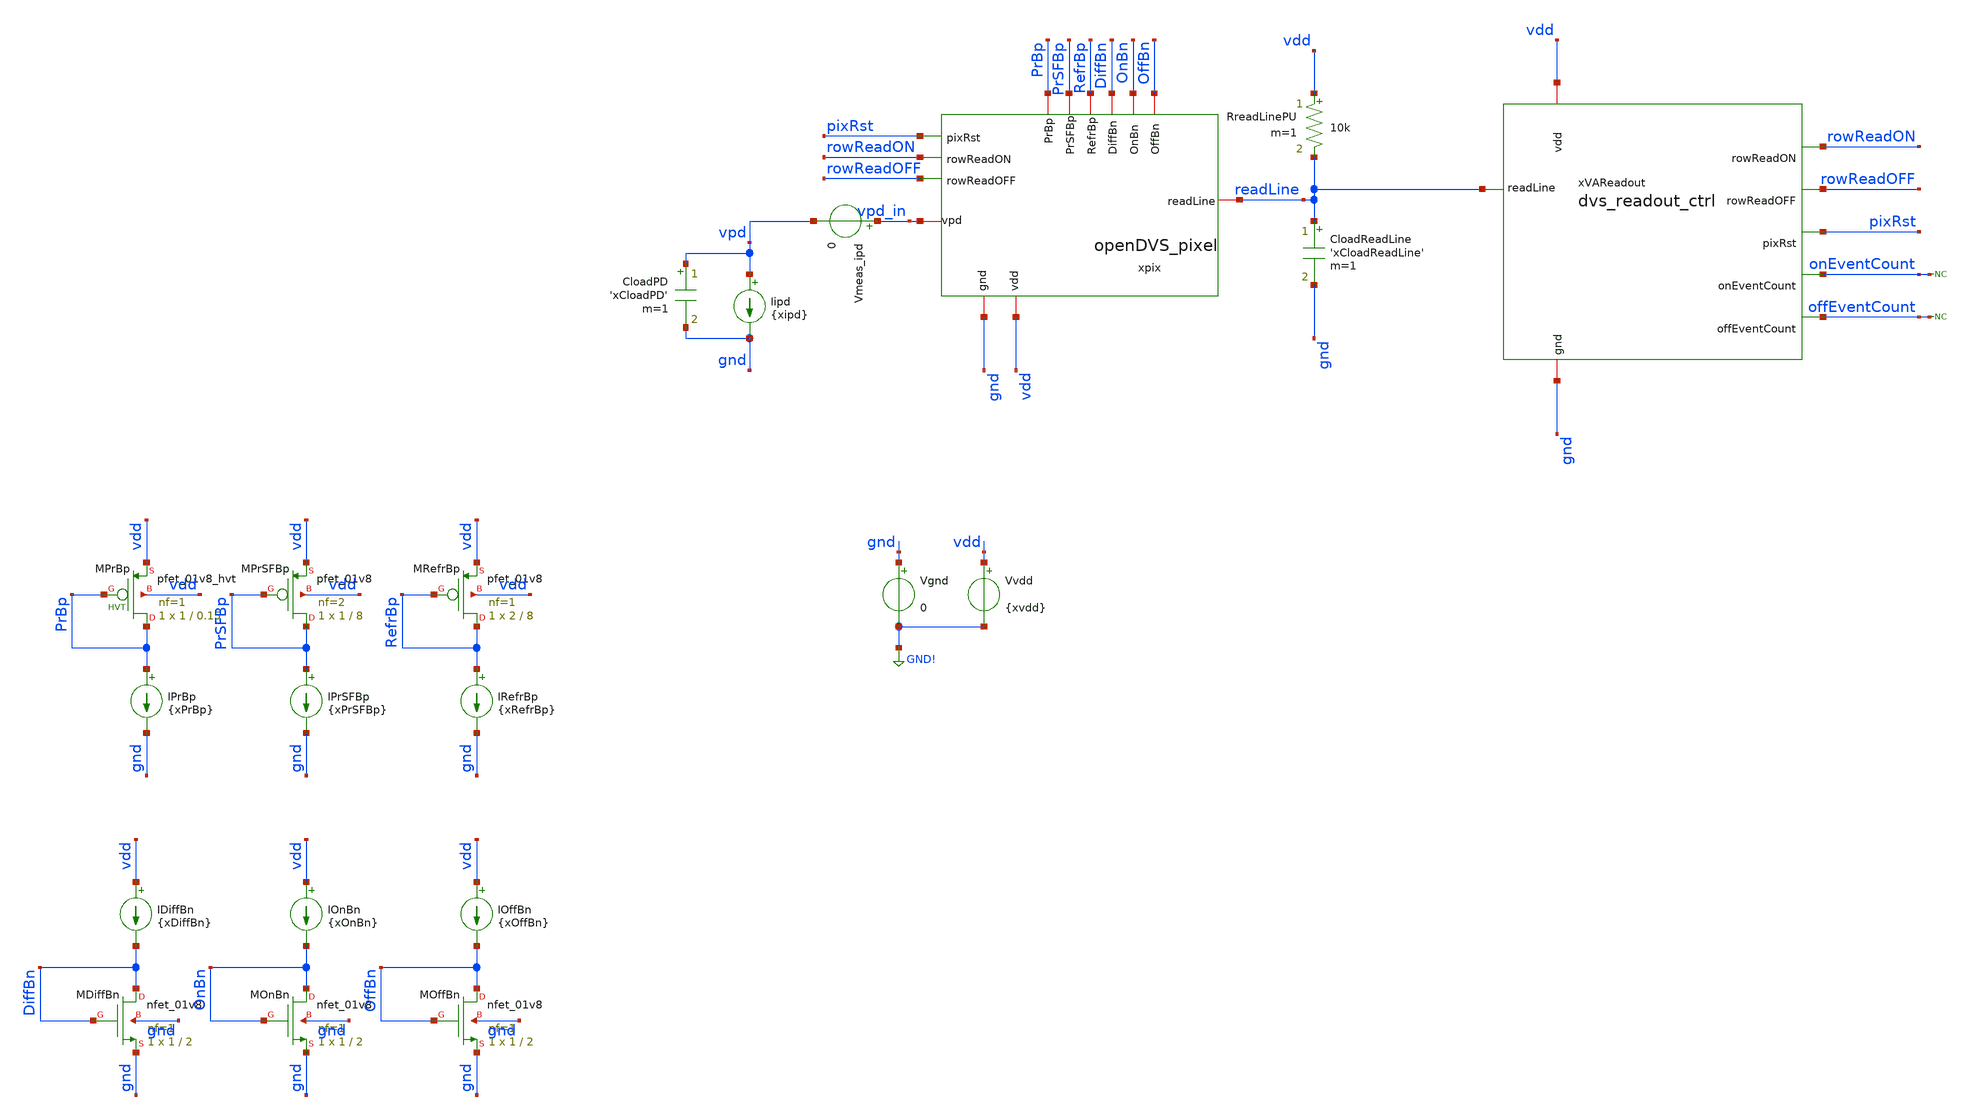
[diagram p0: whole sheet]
** sch_path: analog/klayout/production/final_merge_20260923/testbenches/cace/analog/xschem/pixel_tb.sch
**.subckt pixel_tb
xpix rowReadON vdd PrBp gnd vpd_in rowReadOFF pixRst PrSFBp DiffBn OnBn OffBn RefrBp readLine
+ openDVS_pixel
Vgnd gnd GND! 0
Vvdd vdd GND! {xvdd}
Iipd vpd gnd {xipd}
IRefrBp RefrBp gnd {xRefrBp}
XMRefrBp RefrBp RefrBp vdd vdd sky130_fd_pr__pfet_01v8 L=8 W=2 nf=1 ad='int((1 + 1)/2) * 2 / 1 * 0.29'
+ as='int((1 + 2)/2) * 2 / 1 * 0.29' pd='2*int((1 + 1)/2) * (2 / 1 + 0.29)' ps='2*int((1 + 2)/2) * (2 / 1 + 0.29)'
+ nrd='0.29 / 2 ' nrs='0.29 / 2 ' sa=0 sb=0 sd=0 mult=1 m=1
IPrBp PrBp gnd {xPrBp}
XMPrBp PrBp PrBp vdd vdd sky130_fd_pr__pfet_01v8_hvt L=0.15 W=1 nf=1 ad='int((1 + 1)/2) * 1 / 1 * 0.29'
+ as='int((1 + 2)/2) * 1 / 1 * 0.29' pd='2*int((1 + 1)/2) * (1 / 1 + 0.29)' ps='2*int((1 + 2)/2) * (1 / 1 + 0.29)'
+ nrd='0.29 / 1 ' nrs='0.29 / 1 ' sa=0 sb=0 sd=0 mult=1 m=1
IPrSFBp PrSFBp gnd {xPrSFBp}
XMDiffBn DiffBn DiffBn gnd gnd sky130_fd_pr__nfet_01v8 L=2 W=1 nf=1 ad='int((1 + 1)/2) * 1 / 1 * 0.29'
+ as='int((1 + 2)/2) * 1 / 1 * 0.29' pd='2*int((1 + 1)/2) * (1 / 1 + 0.29)' ps='2*int((1 + 2)/2) * (1 / 1 + 0.29)'
+ nrd='0.29 / 1 ' nrs='0.29 / 1 ' sa=0 sb=0 sd=0 mult=1 m=1
IDiffBn vdd DiffBn {xDiffBn}
XMOnBn OnBn OnBn gnd gnd sky130_fd_pr__nfet_01v8 L=2 W=1 nf=1 ad='int((1 + 1)/2) * 1 / 1 * 0.29' as='int((1 + 2)/2) * 1 / 1 * 0.29'
+ pd='2*int((1 + 1)/2) * (1 / 1 + 0.29)' ps='2*int((1 + 2)/2) * (1 / 1 + 0.29)' nrd='0.29 / 1 ' nrs='0.29 / 1 '
+ sa=0 sb=0 sd=0 mult=1 m=1
IOnBn vdd OnBn {xOnBn}
XMOffBn OffBn OffBn gnd gnd sky130_fd_pr__nfet_01v8 L=2 W=1 nf=1 ad='int((1 + 1)/2) * 1 / 1 * 0.29' as='int((1 + 2)/2) * 1 / 1 * 0.29'
+ pd='2*int((1 + 1)/2) * (1 / 1 + 0.29)' ps='2*int((1 + 2)/2) * (1 / 1 + 0.29)' nrd='0.29 / 1 ' nrs='0.29 / 1 '
+ sa=0 sb=0 sd=0 mult=1 m=1
IOffBn vdd OffBn {xOffBn}
CloadReadLine readLine gnd 'xCloadReadLine' m=1
CloadPD vpd gnd 'xCloadPD' m=1
Vmeas_ipd vpd_in vpd 0
XMPrSFBp PrSFBp PrSFBp vdd vdd sky130_fd_pr__pfet_01v8 L=8 W=1 nf=2 ad='int((2 + 1)/2) * 1 / 2 * 0.29'
+ as='int((2 + 2)/2) * 1 / 2 * 0.29' pd='2*int((2 + 1)/2) * (1 / 2 + 0.29)' ps='2*int((2 + 2)/2) * (1 / 2 + 0.29)'
+ nrd='0.29 / 1 ' nrs='0.29 / 1 ' sa=0 sb=0 sd=0 mult=1 m=1
RreadLinePU vdd readLine 10k m=1
xVAReadout readLine rowReadON rowReadOFF pixRst onEventCount offEventCount vdd gnd dvs_readout_ctrl
* noconn onEventCount
* noconn offEventCount
**** begin user architecture code

** opencircuitdesign pdks install
.lib $::SKYWATER_MODELS/sky130.lib.spice tt



.include /home/rpgraca/research/projects/telluride/2025/nic_eventcam/nic2025_openDVS/analog/xschem/dvs_readout_ctrl.spice

** Convergence options for nA-range weak-inversion pixel circuit
** gmin=1e-15: at 1V node this is 1fA shunt, negligible vs nA signals
** method=gear: damps numerical ringing on stiff circuits (fast digital + slow analog)
** trtol=1: conservative timestep control prevents overshoot at edges
.option gmin=1e-16 abstol=1e-15 vntol=1e-9 reltol=1e-4 chgtol=1e-16
.option method=gear maxord=2 trtol=1
.option itl1=500 itl2=200 itl4=50
.option gminsteps=200 srcsteps=200
.option ramptime=100n

.param xvdd = 1.8
.param xipd = 1e-9
.param xPrBp = 10n
.param xPrSFBp = 100p
.param xRefrBp = 4n
.param xDiffBn = 10n
.param xOnBn = 100n
.param xOffBn = 1n

.param xtr = 1n
.param xtperRead = 3u
.param xtdReadON = 100n
.param xtlenReadON = 950n
.param xtlenReadOFF = 950n
.param xtlenRstPhase = 950n
.param xtdReadOFF = 'xtdReadON+xtlenReadON+10n'
.param xtdRstPhase = 'xtdReadOFF+xtlenReadOFF+10n'
.param xtdRowSel = 50n
.param xtperRowSel = '2*xtperRead'

.param xCloadPD = 30f
.param xCloadReadLine = 300f
.param xCloadRowReadON = 300f
.param xCloadRowReadOFF = 300f
.param xCloadPixRst = 300f

*Small Iphoto testing
Iphoto1 vpd gnd pulse(50n 100n 120m 50m 50m 59.9m 300m)
Iphoto2 vpd gnd pulse(50n 25n 240m 50m 50m 59.9m 300m)

.control

	save all
	op
	tran 100n 390m
        write pixel_tb.raw
.endc


**** end user architecture code
**.ends

* expanding   symbol:  openDVS_pixel.sym # of pins=13
** sym_path: analog/xschem/openDVS_pixel.sym
** sch_path: analog/xschem/openDVS_pixel.sch
.subckt openDVS_pixel rowReadON vdd PrBp gnd vpd rowReadOFF pixRst PrSFBp DiffBn OnBn OffBn RefrBp
+ readLine
*.ipin rowReadON
*.iopin PrBp
*.iopin vdd
*.iopin vpd
*.iopin PrSFBp
*.iopin gnd
*.iopin DiffBn
*.iopin OnBn
*.iopin OffBn
*.ipin rowReadOFF
*.iopin readLine
*.ipin pixRst
*.iopin RefrBp
XC1 vsf vd sky130_fd_pr__cap_mim_m3_1 W=1 L=1 MF=16 m=16
XMpd vdd vpr vpd gnd sky130_fd_pr__nfet_01v8 L=0.15 W=0.5 nf=1 ad='int((1 + 1)/2) * 0.5 / 1 * 0.29' as='int((1 + 2)/2) * 0.5 / 1 * 0.29'
+ pd='2*int((1 + 1)/2) * (0.5 / 1 + 0.29)' ps='2*int((1 + 2)/2) * (0.5 / 1 + 0.29)' nrd='0.29 / 0.5 ' nrs='0.29 / 0.5 '
+ sa=0 sb=0 sd=0 mult=1 m=1
XMpr_amp vpr vpd gnd gnd sky130_fd_pr__nfet_01v8 L=0.15 W=0.5 nf=1 ad='int((1 + 1)/2) * 0.5 / 1 * 0.29'
+ as='int((1 + 2)/2) * 0.5 / 1 * 0.29' pd='2*int((1 + 1)/2) * (0.5 / 1 + 0.29)' ps='2*int((1 + 2)/2) * (0.5 / 1 + 0.29)'
+ nrd='0.29 / 0.5 ' nrs='0.29 / 0.5 ' sa=0 sb=0 sd=0 mult=1 m=1
XD1 gnd vpd sky130_fd_pr__photodiode area=25 perim=20
XC2 vd vdiff sky130_fd_pr__cap_mim_m3_1 W=1 L=1 MF=2 m=2
XMchAmpBias vdiff DiffBn gnd gnd sky130_fd_pr__nfet_01v8 L=2 W=1 nf=1 ad='int((1 + 1)/2) * 1 / 1 * 0.29'
+ as='int((1 + 2)/2) * 1 / 1 * 0.29' pd='2*int((1 + 1)/2) * (1 / 1 + 0.29)' ps='2*int((1 + 2)/2) * (1 / 1 + 0.29)'
+ nrd='0.29 / 1 ' nrs='0.29 / 1 ' sa=0 sb=0 sd=0 mult=1 m=1
XMonBias ON OnBn gnd gnd sky130_fd_pr__nfet_01v8 L=2 W=1 nf=1 ad='int((1 + 1)/2) * 1 / 1 * 0.29' as='int((1 + 2)/2) * 1 / 1 * 0.29'
+ pd='2*int((1 + 1)/2) * (1 / 1 + 0.29)' ps='2*int((1 + 2)/2) * (1 / 1 + 0.29)' nrd='0.29 / 1 ' nrs='0.29 / 1 '
+ sa=0 sb=0 sd=0 mult=1 m=1
XMoffBias nOFF OffBn gnd gnd sky130_fd_pr__nfet_01v8 L=2 W=1 nf=1 ad='int((1 + 1)/2) * 1 / 1 * 0.29'
+ as='int((1 + 2)/2) * 1 / 1 * 0.29' pd='2*int((1 + 1)/2) * (1 / 1 + 0.29)' ps='2*int((1 + 2)/2) * (1 / 1 + 0.29)'
+ nrd='0.29 / 1 ' nrs='0.29 / 1 ' sa=0 sb=0 sd=0 mult=1 m=1
XMswON readLine rowReadON readLineONpd gnd sky130_fd_pr__nfet_01v8 L=0.15 W=0.5 nf=1 ad='int((1 + 1)/2) * 0.5 / 1 * 0.29'
+ as='int((1 + 2)/2) * 0.5 / 1 * 0.29' pd='2*int((1 + 1)/2) * (0.5 / 1 + 0.29)' ps='2*int((1 + 2)/2) * (0.5 / 1 + 0.29)'
+ nrd='0.29 / 0.5 ' nrs='0.29 / 0.5 ' sa=0 sb=0 sd=0 mult=1 m=1
XMoutON readLineONpd ON gnd gnd sky130_fd_pr__nfet_01v8 L=0.15 W=0.5 nf=1 ad='int((1 + 1)/2) * 0.5 / 1 * 0.29'
+ as='int((1 + 2)/2) * 0.5 / 1 * 0.29' pd='2*int((1 + 1)/2) * (0.5 / 1 + 0.29)' ps='2*int((1 + 2)/2) * (0.5 / 1 + 0.29)'
+ nrd='0.29 / 0.5 ' nrs='0.29 / 0.5 ' sa=0 sb=0 sd=0 mult=1 m=1
XMswOFF readLine rowReadOFF readLineOFFpd gnd sky130_fd_pr__nfet_01v8 L=0.15 W=0.5 nf=1 ad='int((1 + 1)/2) * 0.5 / 1 * 0.29'
+ as='int((1 + 2)/2) * 0.5 / 1 * 0.29' pd='2*int((1 + 1)/2) * (0.5 / 1 + 0.29)' ps='2*int((1 + 2)/2) * (0.5 / 1 + 0.29)'
+ nrd='0.29 / 0.5 ' nrs='0.29 / 0.5 ' sa=0 sb=0 sd=0 mult=1 m=1
XMoutOFF readLineOFFpd nOFF gnd gnd sky130_fd_pr__nfet_01v8 L=0.15 W=0.5 nf=1 ad='int((1 + 1)/2) * 0.5 / 1 * 0.29'
+ as='int((1 + 2)/2) * 0.5 / 1 * 0.29' pd='2*int((1 + 1)/2) * (0.5 / 1 + 0.29)' ps='2*int((1 + 2)/2) * (0.5 / 1 + 0.29)'
+ nrd='0.29 / 0.5 ' nrs='0.29 / 0.5 ' sa=0 sb=0 sd=0 mult=1 m=1
XMrst vdiff nRst vd vdd sky130_fd_pr__pfet_01v8_hvt L=0.15 W=1 nf=1 ad='int((1 + 1)/2) * 1 / 1 * 0.29'
+ as='int((1 + 2)/2) * 1 / 1 * 0.29' pd='2*int((1 + 1)/2) * (1 / 1 + 0.29)' ps='2*int((1 + 2)/2) * (1 / 1 + 0.29)'
+ nrd='0.29 / 1 ' nrs='0.29 / 1 ' sa=0 sb=0 sd=0 mult=1 m=1
XMprBias vpr PrBp vdd vdd sky130_fd_pr__pfet_01v8_hvt L=0.15 W=1 nf=1 ad='int((1 + 1)/2) * 1 / 1 * 0.29'
+ as='int((1 + 2)/2) * 1 / 1 * 0.29' pd='2*int((1 + 1)/2) * (1 / 1 + 0.29)' ps='2*int((1 + 2)/2) * (1 / 1 + 0.29)'
+ nrd='0.29 / 1 ' nrs='0.29 / 1 ' sa=0 sb=0 sd=0 mult=1 m=1
XMsfBias vsf PrSFBp vdd vdd sky130_fd_pr__pfet_01v8_hvt L=8 W=2 nf=1 ad='int((1 + 1)/2) * 2 / 1 * 0.29'
+ as='int((1 + 2)/2) * 2 / 1 * 0.29' pd='2*int((1 + 1)/2) * (2 / 1 + 0.29)' ps='2*int((1 + 2)/2) * (2 / 1 + 0.29)'
+ nrd='0.29 / 2 ' nrs='0.29 / 2 ' sa=0 sb=0 sd=0 mult=1 m=1
XMchAmp vdiff vd vdd vdd sky130_fd_pr__pfet_01v8_hvt L=2 W=1 nf=1 ad='int((1 + 1)/2) * 1 / 1 * 0.29'
+ as='int((1 + 2)/2) * 1 / 1 * 0.29' pd='2*int((1 + 1)/2) * (1 / 1 + 0.29)' ps='2*int((1 + 2)/2) * (1 / 1 + 0.29)'
+ nrd='0.29 / 1 ' nrs='0.29 / 1 ' sa=0 sb=0 sd=0 mult=1 m=1
XMon ON vdiff vdd vdd sky130_fd_pr__pfet_01v8_hvt L=2 W=1 nf=1 ad='int((1 + 1)/2) * 1 / 1 * 0.29' as='int((1 + 2)/2) * 1 / 1 * 0.29'
+ pd='2*int((1 + 1)/2) * (1 / 1 + 0.29)' ps='2*int((1 + 2)/2) * (1 / 1 + 0.29)' nrd='0.29 / 1 ' nrs='0.29 / 1 '
+ sa=0 sb=0 sd=0 mult=1 m=1
XMoff nOFF vdiff vdd vdd sky130_fd_pr__pfet_01v8_hvt L=2 W=1 nf=1 ad='int((1 + 1)/2) * 1 / 1 * 0.29'
+ as='int((1 + 2)/2) * 1 / 1 * 0.29' pd='2*int((1 + 1)/2) * (1 / 1 + 0.29)' ps='2*int((1 + 2)/2) * (1 / 1 + 0.29)'
+ nrd='0.29 / 1 ' nrs='0.29 / 1 ' sa=0 sb=0 sd=0 mult=1 m=1
XMrefrInv nRst pixRst gnd gnd sky130_fd_pr__nfet_01v8 L=0.15 W=0.5 nf=1 ad='int((1 + 1)/2) * 0.5 / 1 * 0.29'
+ as='int((1 + 2)/2) * 0.5 / 1 * 0.29' pd='2*int((1 + 1)/2) * (0.5 / 1 + 0.29)' ps='2*int((1 + 2)/2) * (0.5 / 1 + 0.29)'
+ nrd='0.29 / 0.5 ' nrs='0.29 / 0.5 ' sa=0 sb=0 sd=0 mult=1 m=1
XMrefrBias nRst RefrBp vdd vdd sky130_fd_pr__pfet_01v8_hvt L=8 W=2 nf=1 ad='int((1 + 1)/2) * 2 / 1 * 0.29'
+ as='int((1 + 2)/2) * 2 / 1 * 0.29' pd='2*int((1 + 1)/2) * (2 / 1 + 0.29)' ps='2*int((1 + 2)/2) * (2 / 1 + 0.29)'
+ nrd='0.29 / 2 ' nrs='0.29 / 2 ' sa=0 sb=0 sd=0 mult=1 m=1
XMcapRefr vdd nRst net1 vdd sky130_fd_pr__pfet_01v8_hvt L=8 W=8 nf=1 ad='int((1 + 1)/2) * 8 / 1 * 0.29'
+ as='int((1 + 2)/2) * 8 / 1 * 0.29' pd='2*int((1 + 1)/2) * (8 / 1 + 0.29)' ps='2*int((1 + 2)/2) * (8 / 1 + 0.29)'
+ nrd='0.29 / 8 ' nrs='0.29 / 8 ' sa=0 sb=0 sd=0 mult=1 m=1
XMsfBias1 gnd vpr vsf vdd sky130_fd_pr__pfet_01v8_hvt L=2 W=1 nf=1 ad='int((1 + 1)/2) * 1 / 1 * 0.29'
+ as='int((1 + 2)/2) * 1 / 1 * 0.29' pd='2*int((1 + 1)/2) * (1 / 1 + 0.29)' ps='2*int((1 + 2)/2) * (1 / 1 + 0.29)'
+ nrd='0.29 / 1 ' nrs='0.29 / 1 ' sa=0 sb=0 sd=0 mult=1 m=1
.ends

.GLOBAL GND!
.end
